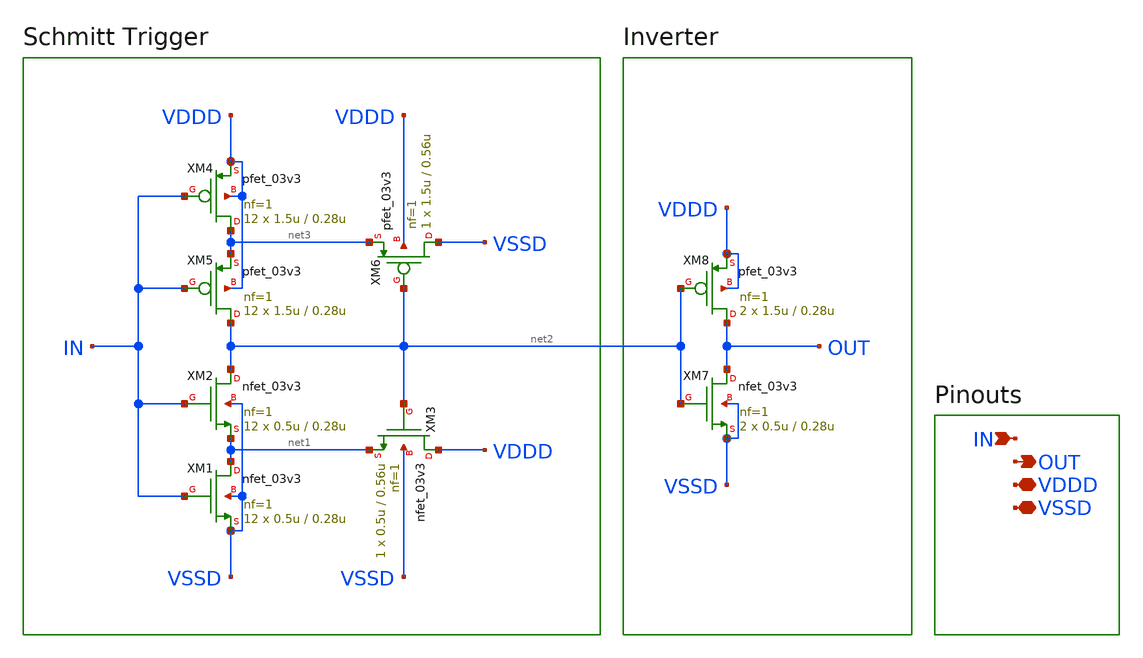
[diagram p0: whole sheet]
** sch_path: designs/libs/core_switch_matrix/schmitt_trigger/schmitt_trigger.sch
**.subckt schmitt_trigger IN OUT VDDD VSSD
*.ipin IN
*.opin OUT
*.iopin VDDD
*.iopin VSSD
XM1 net1 IN VSSD VSSD nfet_03v3 L=0.28u W=0.5u nf=1 ad='int((nf+1)/2) * W/nf * 0.18u' as='int((nf+2)/2) * W/nf * 0.18u'
+ pd='2*int((nf+1)/2) * (W/nf + 0.18u)' ps='2*int((nf+2)/2) * (W/nf + 0.18u)' nrd='0.18u / W' nrs='0.18u / W'
+ sa=0 sb=0 sd=0 m=12
XM2 net2 IN net1 VSSD nfet_03v3 L=0.28u W=0.5u nf=1 ad='int((nf+1)/2) * W/nf * 0.18u' as='int((nf+2)/2) * W/nf * 0.18u'
+ pd='2*int((nf+1)/2) * (W/nf + 0.18u)' ps='2*int((nf+2)/2) * (W/nf + 0.18u)' nrd='0.18u / W' nrs='0.18u / W'
+ sa=0 sb=0 sd=0 m=12
XM3 VDDD net2 net1 VSSD nfet_03v3 L=0.56u W=0.5u nf=1 ad='int((nf+1)/2) * W/nf * 0.18u' as='int((nf+2)/2) * W/nf * 0.18u'
+ pd='2*int((nf+1)/2) * (W/nf + 0.18u)' ps='2*int((nf+2)/2) * (W/nf + 0.18u)' nrd='0.18u / W' nrs='0.18u / W'
+ sa=0 sb=0 sd=0 m=1
XM4 net3 IN VDDD VDDD pfet_03v3 L=0.28u W=1.5u nf=1 ad='int((nf+1)/2) * W/nf * 0.18u' as='int((nf+2)/2) * W/nf * 0.18u'
+ pd='2*int((nf+1)/2) * (W/nf + 0.18u)' ps='2*int((nf+2)/2) * (W/nf + 0.18u)' nrd='0.18u / W' nrs='0.18u / W'
+ sa=0 sb=0 sd=0 m=12
XM5 net2 IN net3 VDDD pfet_03v3 L=0.28u W=1.5u nf=1 ad='int((nf+1)/2) * W/nf * 0.18u' as='int((nf+2)/2) * W/nf * 0.18u'
+ pd='2*int((nf+1)/2) * (W/nf + 0.18u)' ps='2*int((nf+2)/2) * (W/nf + 0.18u)' nrd='0.18u / W' nrs='0.18u / W'
+ sa=0 sb=0 sd=0 m=12
XM6 VSSD net2 net3 VDDD pfet_03v3 L=0.56u W=1.5u nf=1 ad='int((nf+1)/2) * W/nf * 0.18u' as='int((nf+2)/2) * W/nf * 0.18u'
+ pd='2*int((nf+1)/2) * (W/nf + 0.18u)' ps='2*int((nf+2)/2) * (W/nf + 0.18u)' nrd='0.18u / W' nrs='0.18u / W'
+ sa=0 sb=0 sd=0 m=1
XM7 OUT net2 VSSD VSSD nfet_03v3 L=0.28u W=0.5u nf=1 ad='int((nf+1)/2) * W/nf * 0.18u' as='int((nf+2)/2) * W/nf * 0.18u'
+ pd='2*int((nf+1)/2) * (W/nf + 0.18u)' ps='2*int((nf+2)/2) * (W/nf + 0.18u)' nrd='0.18u / W' nrs='0.18u / W'
+ sa=0 sb=0 sd=0 m=2
XM8 OUT net2 VDDD VDDD pfet_03v3 L=0.28u W=1.5u nf=1 ad='int((nf+1)/2) * W/nf * 0.18u' as='int((nf+2)/2) * W/nf * 0.18u'
+ pd='2*int((nf+1)/2) * (W/nf + 0.18u)' ps='2*int((nf+2)/2) * (W/nf + 0.18u)' nrd='0.18u / W' nrs='0.18u / W'
+ sa=0 sb=0 sd=0 m=2
**.ends
.end
